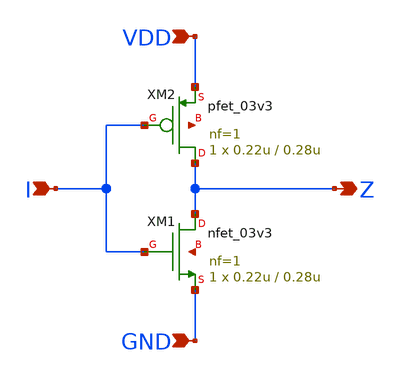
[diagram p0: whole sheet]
** sch_path: 3_Examples/Inverter_Design/Inverter.sch
**.subckt Inverter I Z VDD GND
*.ipin I
*.opin Z
*.ipin VDD
*.ipin GND
XM1 Z I GND net1 nfet_03v3 L=0.28u W=0.22u nf=1 ad='int((nf+1)/2) * W/nf * 0.18u' as='int((nf+2)/2) * W/nf * 0.18u'
+ pd='2*int((nf+1)/2) * (W/nf + 0.18u)' ps='2*int((nf+2)/2) * (W/nf + 0.18u)' nrd='0.18u / W' nrs='0.18u / W'
+ sa=0 sb=0 sd=0 m=1 par=1
XM2 Z I VDD net2 pfet_03v3 L=0.28u W=0.22u nf=1 ad='int((nf+1)/2) * W/nf * 0.18u' as='int((nf+2)/2) * W/nf * 0.18u'
+ pd='2*int((nf+1)/2) * (W/nf + 0.18u)' ps='2*int((nf+2)/2) * (W/nf + 0.18u)' nrd='0.18u / W' nrs='0.18u / W'
+ sa=0 sb=0 sd=0 m=1 par=1
**.ends
.end
